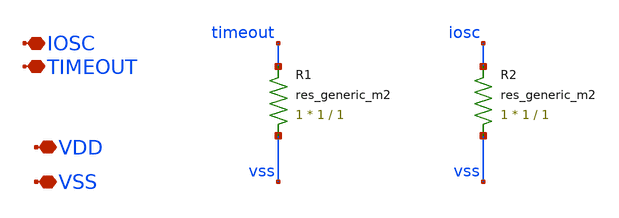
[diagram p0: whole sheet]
** sch_path: images/iic-osic-tools/addons/examples/Open-PMIC-tapeout/xschem/osc_placeholder.sch
**.subckt osc_placeholder IOSC TIMEOUT VDD VSS
*.iopin IOSC
*.iopin TIMEOUT
*.iopin VDD
*.iopin VSS
RR1 vss timeout sky130_fd_pr__res_generic_m2 W=1 L=1 m=1
RR2 vss iosc sky130_fd_pr__res_generic_m2 W=1 L=1 m=1
**.ends
.end
